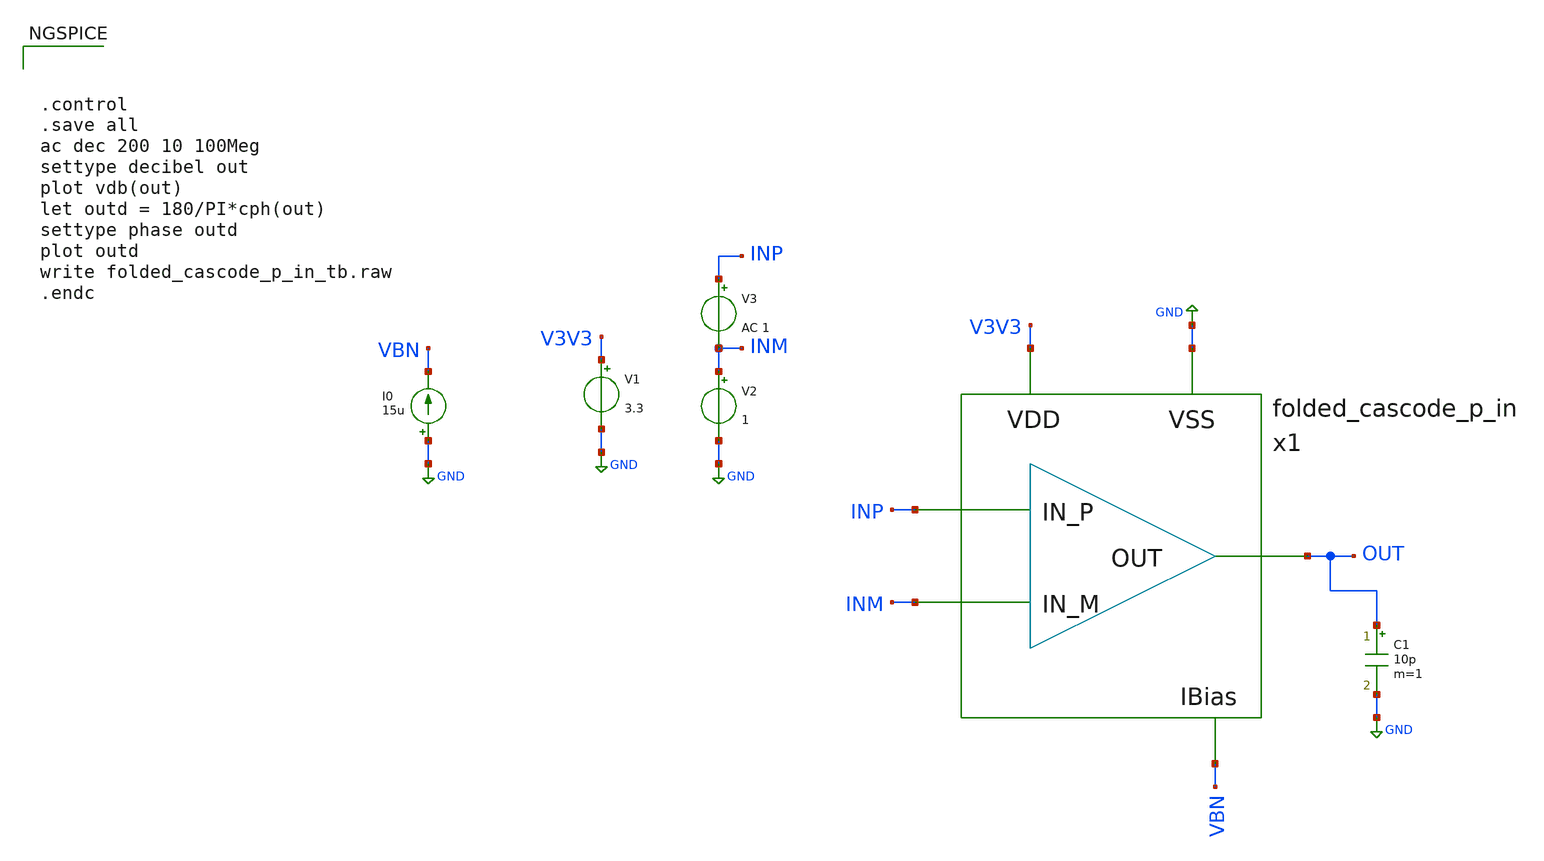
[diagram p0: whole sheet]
** sch_path: design/folded-cascode-p-in/folded_cascode_p_in_tb.sch
**.subckt folded_cascode_p_in_tb
V1 V3V3 GND 3.3
I0 GND VBN 15u
V2 INM GND 1
V3 INP INM AC 1
C1 OUT GND 10p m=1
x1 INP INM OUT V3V3 GND VBN folded_cascode_p_in
**** begin user architecture code



.control
.save all
ac dec 200 10 100Meg
settype decibel out
plot vdb(out)
let outd = 180/PI*cph(out)
settype phase outd
plot outd
write folded_cascode_p_in_tb.raw
.endc



.include $::SKYWATER_MODELS/cells/nfet_01v8/sky130_fd_pr__nfet_01v8__tt.corner.spice
.include $::SKYWATER_MODELS/cells/nfet_01v8_lvt/sky130_fd_pr__nfet_01v8_lvt__tt.corner.spice
.include $::SKYWATER_MODELS/cells/pfet_01v8/sky130_fd_pr__pfet_01v8__tt.corner.spice
.include $::SKYWATER_MODELS/cells/nfet_03v3_nvt/sky130_fd_pr__nfet_03v3_nvt__tt.corner.spice
.include $::SKYWATER_MODELS/cells/nfet_05v0_nvt/sky130_fd_pr__nfet_05v0_nvt__tt.corner.spice
.include $::SKYWATER_MODELS/cells/esd_nfet_01v8/sky130_fd_pr__esd_nfet_01v8__tt.corner.spice
.include $::SKYWATER_MODELS/cells/pfet_01v8_lvt/sky130_fd_pr__pfet_01v8_lvt__tt.corner.spice
.include $::SKYWATER_MODELS/cells/pfet_01v8_hvt/sky130_fd_pr__pfet_01v8_hvt__tt.corner.spice
.include $::SKYWATER_MODELS/cells/esd_pfet_g5v0d10v5/sky130_fd_pr__esd_pfet_g5v0d10v5__tt.corner.spice
.include $::SKYWATER_MODELS/cells/pfet_g5v0d10v5/sky130_fd_pr__pfet_g5v0d10v5__tt.corner.spice
.include $::SKYWATER_MODELS/cells/pfet_g5v0d16v0/sky130_fd_pr__pfet_g5v0d16v0__tt.corner.spice
.include $::SKYWATER_MODELS/cells/nfet_g5v0d10v5/sky130_fd_pr__nfet_g5v0d10v5__tt.corner.spice
.include $::SKYWATER_MODELS/cells/nfet_g5v0d16v0/sky130_fd_pr__nfet_g5v0d16v0__tt_discrete.corner.spice
.include $::SKYWATER_MODELS/cells/esd_nfet_g5v0d10v5/sky130_fd_pr__esd_nfet_g5v0d10v5__tt.corner.spice
.include $::SKYWATER_MODELS/models/corners/tt/nonfet.spice
* Mismatch parameters
.include $::SKYWATER_MODELS/cells/nfet_01v8/sky130_fd_pr__nfet_01v8__mismatch.corner.spice
.include $::SKYWATER_MODELS/cells/pfet_01v8/sky130_fd_pr__pfet_01v8__mismatch.corner.spice
.include $::SKYWATER_MODELS/cells/nfet_01v8_lvt/sky130_fd_pr__nfet_01v8_lvt__mismatch.corner.spice
.include $::SKYWATER_MODELS/cells/pfet_01v8_lvt/sky130_fd_pr__pfet_01v8_lvt__mismatch.corner.spice
.include $::SKYWATER_MODELS/cells/pfet_01v8_hvt/sky130_fd_pr__pfet_01v8_hvt__mismatch.corner.spice
.include $::SKYWATER_MODELS/cells/nfet_g5v0d10v5/sky130_fd_pr__nfet_g5v0d10v5__mismatch.corner.spice
.include $::SKYWATER_MODELS/cells/pfet_g5v0d10v5/sky130_fd_pr__pfet_g5v0d10v5__mismatch.corner.spice
.include $::SKYWATER_MODELS/cells/nfet_05v0_nvt/sky130_fd_pr__nfet_05v0_nvt__mismatch.corner.spice
.include $::SKYWATER_MODELS/cells/nfet_03v3_nvt/sky130_fd_pr__nfet_03v3_nvt__mismatch.corner.spice
* Resistor$::SKYWATER_MODELS/Capacitor
.include $::SKYWATER_MODELS/models/r+c/res_typical__cap_typical.spice
.include $::SKYWATER_MODELS/models/r+c/res_typical__cap_typical__lin.spice
* Special cells
.include $::SKYWATER_MODELS/models/corners/tt/specialized_cells.spice
* All models
.include $::SKYWATER_MODELS/models/all.spice
* Corner
.include $::SKYWATER_MODELS/models/corners/tt/rf.spice

**** end user architecture code
**.ends

* expanding   symbol:  design/folded-cascode-p-in/folded_cascode_p_in.sym # of pins=6
** sym_path: design/folded-cascode-p-in/folded_cascode_p_in.sym
** sch_path: design/folded-cascode-p-in/folded_cascode_p_in.sch
.subckt folded_cascode_p_in IN_P IN_M OUT VDD VSS VBN
*.ipin IN_P
*.ipin IN_M
*.ipin OUT
*.ipin VDD
*.ipin VSS
*.ipin VBN
XM7 net4 VBP VDD VDD sky130_fd_pr__pfet_g5v0d10v5 L=1 W=5 nf=1 ad='int((nf+1)/2) * W/nf * 0.29' as='int((nf+2)/2) * W/nf * 0.29'
+ pd='2*int((nf+1)/2) * (W/nf + 0.29)' ps='2*int((nf+2)/2) * (W/nf + 0.29)' nrd='0.29 / W' nrs='0.29 / W'
+ sa=0 sb=0 sd=0 mult=12 m=12
XM8 VS1_P IN_M net4 VDD sky130_fd_pr__pfet_g5v0d10v5 L=1 W=5 nf=1 ad='int((nf+1)/2) * W/nf * 0.29' as='int((nf+2)/2) * W/nf * 0.29'
+ pd='2*int((nf+1)/2) * (W/nf + 0.29)' ps='2*int((nf+2)/2) * (W/nf + 0.29)' nrd='0.29 / W' nrs='0.29 / W'
+ sa=0 sb=0 sd=0 mult=24 m=24
XM15 VS1_M IN_P net4 VDD sky130_fd_pr__pfet_g5v0d10v5 L=1 W=5 nf=1 ad='int((nf+1)/2) * W/nf * 0.29' as='int((nf+2)/2) * W/nf * 0.29'
+ pd='2*int((nf+1)/2) * (W/nf + 0.29)' ps='2*int((nf+2)/2) * (W/nf + 0.29)' nrd='0.29 / W' nrs='0.29 / W'
+ sa=0 sb=0 sd=0 mult=24 m=24
XM16 VS1_P VBN_INT VSS VSS sky130_fd_pr__nfet_g5v0d10v5 L=1 W=5 nf=1 ad='int((nf+1)/2) * W/nf * 0.29'
+ as='int((nf+2)/2) * W/nf * 0.29' pd='2*int((nf+1)/2) * (W/nf + 0.29)' ps='2*int((nf+2)/2) * (W/nf + 0.29)'
+ nrd='0.29 / W' nrs='0.29 / W' sa=0 sb=0 sd=0 mult=9 m=9
XM20 VS1_M VBN_INT VSS VSS sky130_fd_pr__nfet_g5v0d10v5 L=1 W=5 nf=1 ad='int((nf+1)/2) * W/nf * 0.29'
+ as='int((nf+2)/2) * W/nf * 0.29' pd='2*int((nf+1)/2) * (W/nf + 0.29)' ps='2*int((nf+2)/2) * (W/nf + 0.29)'
+ nrd='0.29 / W' nrs='0.29 / W' sa=0 sb=0 sd=0 mult=9 m=9
XM22 net3 VCP net1 VDD sky130_fd_pr__pfet_g5v0d10v5 L=1 W=5 nf=1 ad='int((nf+1)/2) * W/nf * 0.29' as='int((nf+2)/2) * W/nf * 0.29'
+ pd='2*int((nf+1)/2) * (W/nf + 0.29)' ps='2*int((nf+2)/2) * (W/nf + 0.29)' nrd='0.29 / W' nrs='0.29 / W'
+ sa=0 sb=0 sd=0 mult=3 m=3
XM23 net1 net3 VDD VDD sky130_fd_pr__pfet_g5v0d10v5 L=1 W=5 nf=1 ad='int((nf+1)/2) * W/nf * 0.29' as='int((nf+2)/2) * W/nf * 0.29'
+ pd='2*int((nf+1)/2) * (W/nf + 0.29)' ps='2*int((nf+2)/2) * (W/nf + 0.29)' nrd='0.29 / W' nrs='0.29 / W'
+ sa=0 sb=0 sd=0 mult=3 m=3
XM24 OUT VCP net2 VDD sky130_fd_pr__pfet_g5v0d10v5 L=1 W=5 nf=1 ad='int((nf+1)/2) * W/nf * 0.29' as='int((nf+2)/2) * W/nf * 0.29'
+ pd='2*int((nf+1)/2) * (W/nf + 0.29)' ps='2*int((nf+2)/2) * (W/nf + 0.29)' nrd='0.29 / W' nrs='0.29 / W'
+ sa=0 sb=0 sd=0 mult=3 m=3
XM25 net2 net3 VDD VDD sky130_fd_pr__pfet_g5v0d10v5 L=1 W=5 nf=1 ad='int((nf+1)/2) * W/nf * 0.29' as='int((nf+2)/2) * W/nf * 0.29'
+ pd='2*int((nf+1)/2) * (W/nf + 0.29)' ps='2*int((nf+2)/2) * (W/nf + 0.29)' nrd='0.29 / W' nrs='0.29 / W'
+ sa=0 sb=0 sd=0 mult=3 m=3
XM26 OUT VCN VS1_P VSS sky130_fd_pr__nfet_g5v0d10v5 L=1 W=5 nf=1 ad='int((nf+1)/2) * W/nf * 0.29' as='int((nf+2)/2) * W/nf * 0.29'
+ pd='2*int((nf+1)/2) * (W/nf + 0.29)' ps='2*int((nf+2)/2) * (W/nf + 0.29)' nrd='0.29 / W' nrs='0.29 / W'
+ sa=0 sb=0 sd=0 mult=3 m=3
XM27 net3 VCN VS1_M VSS sky130_fd_pr__nfet_g5v0d10v5 L=1 W=5 nf=1 ad='int((nf+1)/2) * W/nf * 0.29' as='int((nf+2)/2) * W/nf * 0.29'
+ pd='2*int((nf+1)/2) * (W/nf + 0.29)' ps='2*int((nf+2)/2) * (W/nf + 0.29)' nrd='0.29 / W' nrs='0.29 / W'
+ sa=0 sb=0 sd=0 mult=3 m=3
XM29 VBN_INT VBN_INT VSS VSS sky130_fd_pr__nfet_g5v0d10v5 L=1 W=5 nf=1 ad='int((nf+1)/2) * W/nf * 0.29'
+ as='int((nf+2)/2) * W/nf * 0.29' pd='2*int((nf+1)/2) * (W/nf + 0.29)' ps='2*int((nf+2)/2) * (W/nf + 0.29)'
+ nrd='0.29 / W' nrs='0.29 / W' sa=0 sb=0 sd=0 mult=1 m=1
XM30 VBN_INT VBP VDD VDD sky130_fd_pr__pfet_g5v0d10v5 L=1 W=5 nf=1 ad='int((nf+1)/2) * W/nf * 0.29' as='int((nf+2)/2) * W/nf * 0.29'
+ pd='2*int((nf+1)/2) * (W/nf + 0.29)' ps='2*int((nf+2)/2) * (W/nf + 0.29)' nrd='0.29 / W' nrs='0.29 / W'
+ sa=0 sb=0 sd=0 mult=1 m=1
XM1 VBP VBP VDD VDD sky130_fd_pr__pfet_g5v0d10v5 L=1 W=5 nf=1 ad='int((nf+1)/2) * W/nf * 0.29' as='int((nf+2)/2) * W/nf * 0.29'
+ pd='2*int((nf+1)/2) * (W/nf + 0.29)' ps='2*int((nf+2)/2) * (W/nf + 0.29)' nrd='0.29 / W' nrs='0.29 / W'
+ sa=0 sb=0 sd=0 mult=1 m=1
XM2 net5 VBP net12 VDD sky130_fd_pr__pfet_g5v0d10v5 L=1 W=5 nf=1 ad='int((nf+1)/2) * W/nf * 0.29' as='int((nf+2)/2) * W/nf * 0.29'
+ pd='2*int((nf+1)/2) * (W/nf + 0.29)' ps='2*int((nf+2)/2) * (W/nf + 0.29)' nrd='0.29 / W' nrs='0.29 / W'
+ sa=0 sb=0 sd=0 mult=1 m=1
XM3 VCN VBP VDD VDD sky130_fd_pr__pfet_g5v0d10v5 L=1 W=5 nf=1 ad='int((nf+1)/2) * W/nf * 0.29' as='int((nf+2)/2) * W/nf * 0.29'
+ pd='2*int((nf+1)/2) * (W/nf + 0.29)' ps='2*int((nf+2)/2) * (W/nf + 0.29)' nrd='0.29 / W' nrs='0.29 / W'
+ sa=0 sb=0 sd=0 mult=1 m=1
XM4 net5 net5 net6 VSS sky130_fd_pr__nfet_g5v0d10v5 L=1 W=5 nf=1 ad='int((nf+1)/2) * W/nf * 0.29' as='int((nf+2)/2) * W/nf * 0.29'
+ pd='2*int((nf+1)/2) * (W/nf + 0.29)' ps='2*int((nf+2)/2) * (W/nf + 0.29)' nrd='0.29 / W' nrs='0.29 / W'
+ sa=0 sb=0 sd=0 mult=2 m=2
XM5 net6 net5 VSS VSS sky130_fd_pr__nfet_g5v0d10v5 L=1 W=5 nf=1 ad='int((nf+1)/2) * W/nf * 0.29' as='int((nf+2)/2) * W/nf * 0.29'
+ pd='2*int((nf+1)/2) * (W/nf + 0.29)' ps='2*int((nf+2)/2) * (W/nf + 0.29)' nrd='0.29 / W' nrs='0.29 / W'
+ sa=0 sb=0 sd=0 mult=1 m=1
XM21 VCN VCN net6 VSS sky130_fd_pr__nfet_g5v0d10v5 L=1 W=5 nf=1 ad='int((nf+1)/2) * W/nf * 0.29' as='int((nf+2)/2) * W/nf * 0.29'
+ pd='2*int((nf+1)/2) * (W/nf + 0.29)' ps='2*int((nf+2)/2) * (W/nf + 0.29)' nrd='0.29 / W' nrs='0.29 / W'
+ sa=0 sb=0 sd=0 mult=1 m=1
XM6 net7 VBN net10 VSS sky130_fd_pr__nfet_g5v0d10v5 L=1 W=5 nf=1 ad='int((nf+1)/2) * W/nf * 0.29' as='int((nf+2)/2) * W/nf * 0.29'
+ pd='2*int((nf+1)/2) * (W/nf + 0.29)' ps='2*int((nf+2)/2) * (W/nf + 0.29)' nrd='0.29 / W' nrs='0.29 / W'
+ sa=0 sb=0 sd=0 mult=1 m=1
XM9 VCP VBN VSS VSS sky130_fd_pr__nfet_g5v0d10v5 L=1 W=5 nf=1 ad='int((nf+1)/2) * W/nf * 0.29' as='int((nf+2)/2) * W/nf * 0.29'
+ pd='2*int((nf+1)/2) * (W/nf + 0.29)' ps='2*int((nf+2)/2) * (W/nf + 0.29)' nrd='0.29 / W' nrs='0.29 / W'
+ sa=0 sb=0 sd=0 mult=1 m=1
XM10 net7 net7 net8 VDD sky130_fd_pr__pfet_g5v0d10v5 L=1 W=5 nf=1 ad='int((nf+1)/2) * W/nf * 0.29' as='int((nf+2)/2) * W/nf * 0.29'
+ pd='2*int((nf+1)/2) * (W/nf + 0.29)' ps='2*int((nf+2)/2) * (W/nf + 0.29)' nrd='0.29 / W' nrs='0.29 / W'
+ sa=0 sb=0 sd=0 mult=2 m=2
XM11 VCP VCP net8 VDD sky130_fd_pr__pfet_g5v0d10v5 L=1 W=5 nf=1 ad='int((nf+1)/2) * W/nf * 0.29' as='int((nf+2)/2) * W/nf * 0.29'
+ pd='2*int((nf+1)/2) * (W/nf + 0.29)' ps='2*int((nf+2)/2) * (W/nf + 0.29)' nrd='0.29 / W' nrs='0.29 / W'
+ sa=0 sb=0 sd=0 mult=1 m=1
XM28 net8 net7 VDD VDD sky130_fd_pr__pfet_g5v0d10v5 L=1 W=5 nf=1 ad='int((nf+1)/2) * W/nf * 0.29' as='int((nf+2)/2) * W/nf * 0.29'
+ pd='2*int((nf+1)/2) * (W/nf + 0.29)' ps='2*int((nf+2)/2) * (W/nf + 0.29)' nrd='0.29 / W' nrs='0.29 / W'
+ sa=0 sb=0 sd=0 mult=1 m=1
XM12 VBP VBN VSS VSS sky130_fd_pr__nfet_g5v0d10v5 L=1 W=5 nf=1 ad='int((nf+1)/2) * W/nf * 0.29' as='int((nf+2)/2) * W/nf * 0.29'
+ pd='2*int((nf+1)/2) * (W/nf + 0.29)' ps='2*int((nf+2)/2) * (W/nf + 0.29)' nrd='0.29 / W' nrs='0.29 / W'
+ sa=0 sb=0 sd=0 mult=1 m=1
XM32 net12 VBP net9 VDD sky130_fd_pr__pfet_g5v0d10v5 L=1 W=5 nf=1 ad='int((nf+1)/2) * W/nf * 0.29' as='int((nf+2)/2) * W/nf * 0.29'
+ pd='2*int((nf+1)/2) * (W/nf + 0.29)' ps='2*int((nf+2)/2) * (W/nf + 0.29)' nrd='0.29 / W' nrs='0.29 / W'
+ sa=0 sb=0 sd=0 mult=1 m=1
XM33 net9 VBP VDD VDD sky130_fd_pr__pfet_g5v0d10v5 L=1 W=5 nf=1 ad='int((nf+1)/2) * W/nf * 0.29' as='int((nf+2)/2) * W/nf * 0.29'
+ pd='2*int((nf+1)/2) * (W/nf + 0.29)' ps='2*int((nf+2)/2) * (W/nf + 0.29)' nrd='0.29 / W' nrs='0.29 / W'
+ sa=0 sb=0 sd=0 mult=1 m=1
XM34 net10 VBN net11 VSS sky130_fd_pr__nfet_g5v0d10v5 L=1 W=5 nf=1 ad='int((nf+1)/2) * W/nf * 0.29' as='int((nf+2)/2) * W/nf * 0.29'
+ pd='2*int((nf+1)/2) * (W/nf + 0.29)' ps='2*int((nf+2)/2) * (W/nf + 0.29)' nrd='0.29 / W' nrs='0.29 / W'
+ sa=0 sb=0 sd=0 mult=1 m=1
XM35 net11 VBN VSS VSS sky130_fd_pr__nfet_g5v0d10v5 L=1 W=5 nf=1 ad='int((nf+1)/2) * W/nf * 0.29' as='int((nf+2)/2) * W/nf * 0.29'
+ pd='2*int((nf+1)/2) * (W/nf + 0.29)' ps='2*int((nf+2)/2) * (W/nf + 0.29)' nrd='0.29 / W' nrs='0.29 / W'
+ sa=0 sb=0 sd=0 mult=1 m=1
XM13 VBN VBN VSS VSS sky130_fd_pr__nfet_g5v0d10v5 L=1 W=5 nf=1 ad='int((nf+1)/2) * W/nf * 0.29' as='int((nf+2)/2) * W/nf * 0.29'
+ pd='2*int((nf+1)/2) * (W/nf + 0.29)' ps='2*int((nf+2)/2) * (W/nf + 0.29)' nrd='0.29 / W' nrs='0.29 / W'
+ sa=0 sb=0 sd=0 mult=1 m=1
XM14 VBN_INT VBN_INT VS1_P VDD sky130_fd_pr__pfet_g5v0d10v5 L=1 W=5 nf=1 ad='int((nf+1)/2) * W/nf * 0.29'
+ as='int((nf+2)/2) * W/nf * 0.29' pd='2*int((nf+1)/2) * (W/nf + 0.29)' ps='2*int((nf+2)/2) * (W/nf + 0.29)'
+ nrd='0.29 / W' nrs='0.29 / W' sa=0 sb=0 sd=0 mult=1 m=1
XM17 VBN_INT VBN_INT VS1_M VDD sky130_fd_pr__pfet_g5v0d10v5 L=1 W=5 nf=1 ad='int((nf+1)/2) * W/nf * 0.29'
+ as='int((nf+2)/2) * W/nf * 0.29' pd='2*int((nf+1)/2) * (W/nf + 0.29)' ps='2*int((nf+2)/2) * (W/nf + 0.29)'
+ nrd='0.29 / W' nrs='0.29 / W' sa=0 sb=0 sd=0 mult=1 m=1
.ends

.GLOBAL GND
**** begin user architecture code
[sky130_models]
**** end user architecture code
.end
